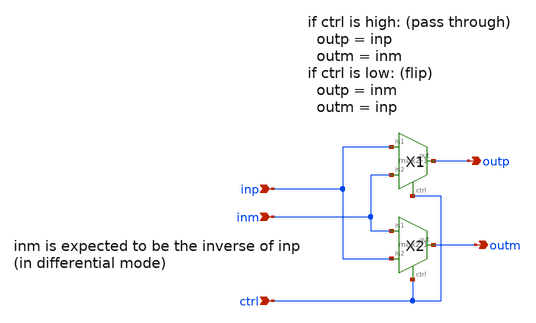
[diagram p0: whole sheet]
** sch_path: xschem/mux/multiplier_differential.sch
**.subckt multiplier_differential inp inm outp outm ctrl
*.ipin inp
*.ipin inm
*.opin outp
*.opin outm
*.ipin ctrl
X1 inp outp inm ctrl mux2-1
X2 inm outm inp ctrl mux2-1
**.ends

* expanding   symbol:  mux/mux2-1.sym # of pins=4
** sym_path: xschem/mux/mux2-1.sym
** sch_path: xschem/mux/mux2-1.sch
.subckt mux2-1 in1 out in2 ctrl
*.ipin in1
*.ipin ctrl
*.ipin in2
*.iopin out
X1 in1 out net1 ctrl transmission_gate Wpmos=3 Lpmos=0.18 Wnmos=1 Lnmos=0.18
X2 in2 out ctrl net1 transmission_gate Wpmos=3 Lpmos=0.18 Wnmos=1 Lnmos=0.18
X4 ctrl net1 inv Wpmos=3 Lpmos=0.18 Wnmos=1 Lnmos=0.18
.ends


* expanding   symbol:  transmission_gate/transmission_gate.sym # of pins=4
** sym_path: xschem/transmission_gate/transmission_gate.sym
** sch_path: xschem/transmission_gate/transmission_gate.sch
.subckt transmission_gate in out ctrl_ ctrl  Wpmos=1 Lpmos=0.18 Wnmos=1 Lnmos=0.18
*.iopin in
*.iopin out
*.ipin ctrl_
*.ipin ctrl
XM1 in ctrl out GND sky130_fd_pr__nfet_01v8 L=Lnmos W=Wnmos nf=1 ad='int((nf+1)/2) * W/nf * 0.29' as='int((nf+2)/2) * W/nf * 0.29'
+ pd='2*int((nf+1)/2) * (W/nf + 0.29)' ps='2*int((nf+2)/2) * (W/nf + 0.29)' nrd='0.29 / W' nrs='0.29 / W'
+ sa=0 sb=0 sd=0 mult=1 m=1
XM2 out ctrl_ in VDD sky130_fd_pr__pfet_01v8 L=Lpmos W=Wpmos nf=1 ad='int((nf+1)/2) * W/nf * 0.29' as='int((nf+2)/2) * W/nf * 0.29'
+ pd='2*int((nf+1)/2) * (W/nf + 0.29)' ps='2*int((nf+2)/2) * (W/nf + 0.29)' nrd='0.29 / W' nrs='0.29 / W'
+ sa=0 sb=0 sd=0 mult=1 m=1
.ends


* expanding   symbol:  inv/inv.sym # of pins=2
** sym_path: xschem/inv/inv.sym
** sch_path: xschem/inv/inv.sch
.subckt inv in out  Wpmos=3 Lpmos=0.18 Wnmos=1 Lnmos=0.18
*.ipin in
*.iopin out
XM1 out in GND GND sky130_fd_pr__nfet_01v8 L=Lnmos W=Wnmos nf=1 ad='int((nf+1)/2) * W/nf * 0.29' as='int((nf+2)/2) * W/nf * 0.29'
+ pd='2*int((nf+1)/2) * (W/nf + 0.29)' ps='2*int((nf+2)/2) * (W/nf + 0.29)' nrd='0.29 / W' nrs='0.29 / W'
+ sa=0 sb=0 sd=0 mult=1 m=1
XM2 out in VDD VDD sky130_fd_pr__pfet_01v8 L=Lpmos W=Wpmos nf=1 ad='int((nf+1)/2) * W/nf * 0.29' as='int((nf+2)/2) * W/nf * 0.29'
+ pd='2*int((nf+1)/2) * (W/nf + 0.29)' ps='2*int((nf+2)/2) * (W/nf + 0.29)' nrd='0.29 / W' nrs='0.29 / W'
+ sa=0 sb=0 sd=0 mult=1 m=1
.ends

.GLOBAL GND
.GLOBAL VDD
.end
